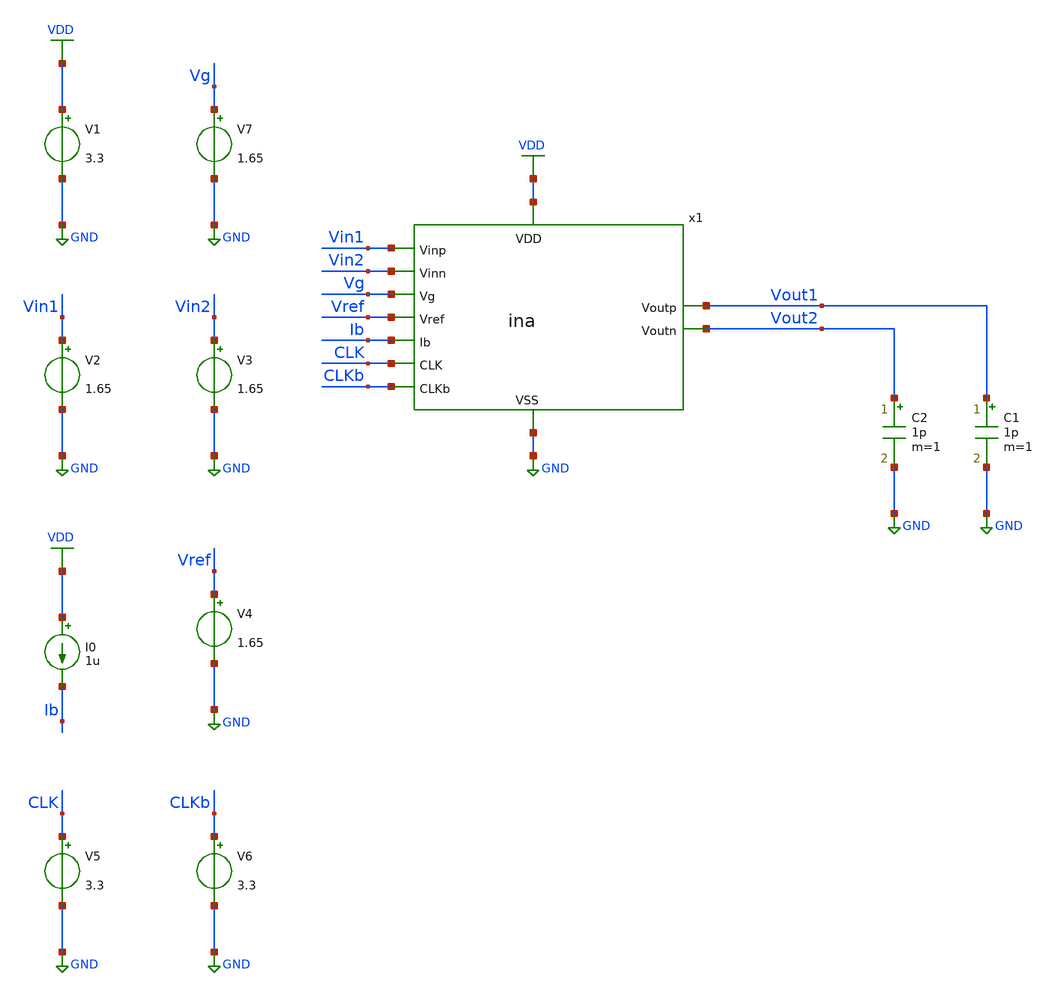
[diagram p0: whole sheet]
** sch_path: designs/libs/tb_ina/tb_ina_tran/tb_ina_tran.sch
**.subckt tb_ina_tran
V1 VDD GND 3.3
V2 Vin1 GND 1.65
V3 Vin2 GND 1.65
C2 Vout2 GND 1p m=1
C1 Vout1 GND 1p m=1
I0 VDD Ib 1u
V4 Vref GND 1.65
x1 Vg VDD Vin1 Vin2 CLK Vout1 CLKb Vout2 GND Vref Ib ina
V5 CLK GND 3.3
V6 CLKb GND 3.3
V7 Vg GND 1.65
**** begin user architecture code

.include $::180MCU_MODELS/design.ngspice
.lib $::180MCU_MODELS/sm141064.ngspice typical
.lib $::180MCU_MODELS/sm141064.ngspice cap_mim
.lib $::180MCU_MODELS/sm141064.ngspice moscap_typical
.lib $::180MCU_MODELS/sm141064.ngspice mimcap_typical
.lib $::180MCU_MODELS/sm141064.ngspice res_typical
* .lib $::180MCU_MODELS/sm141064.ngspice res_statistical
* ngspice commands




.control
save all

run
set color0 = white

*************************************
** ECG INPUT PARAMETERS
*************************************

let Vdd  = 3.3
let Vcm  = 1.65
let Vamp = 0.5m
let fecg = 100

*************************************
** CHOPPER PARAMETERS
*************************************

let fchop = 4k
let tper = 1/fchop
let td = 1u
let ton = tper/2-td
let tdclk = td/2
let tdclkb = tper/2+td/2
let tr = 10n
let tf = 10n

*************************************
** BIAS PARAMETERS
*************************************

let Ibias = 1u
let Vref  = 1.65
let Vg 	  = 1.65

*************************************
** TRANSIENT PARAMETERS
*************************************

let tstop = 20m
let tstep = 500n

*************************************
** SOURCES
*************************************

alter @V1[DC] = $&Vdd
alter @V2[SIN] = [ $&Vcm $&Vamp $&fecg ]
alter @V3[SIN] = [ $&Vcm -$&Vamp $&fecg ]
alter @V4[DC] = $&Vref
alter @I0[DC] = $&Ibias
alter @V5[PULSE] = [ 0 $&Vdd $&tdclk $&tr $&tf $&ton $&tper 0 ]
alter @V6[PULSE] = [ 0 $&Vdd $&tdclkb $&tr $&tf $&ton $&tper 0 ]
alter @V7[DC] = $&Vg

*************************************
** TRANSIENT SIMULATION
*************************************

tran $&tstep $&tstop

*************************************
** PLOTS
*************************************

setplot tran1
let vin1 = v(Vin1)
let vin2 = v(Vin2)
let vout1 = v(Vout1)
let vout2 = v(Vout2)
let vin_diff  = vin1-vin2
let vout_diff = vout1-vout2
let vclk = v(CLK)
let vclkb = v(CLKb)
plot vclk vclkb
plot vin1 vin2
plot vin_diff
plot vout1 vout2
plot vout_diff

*************************************
** SAVE
*************************************

write tb_ina_tran.raw

.endc
* ngspice commands



**** end user architecture code
**.ends
.GLOBAL GND
.GLOBAL VDD
.end
